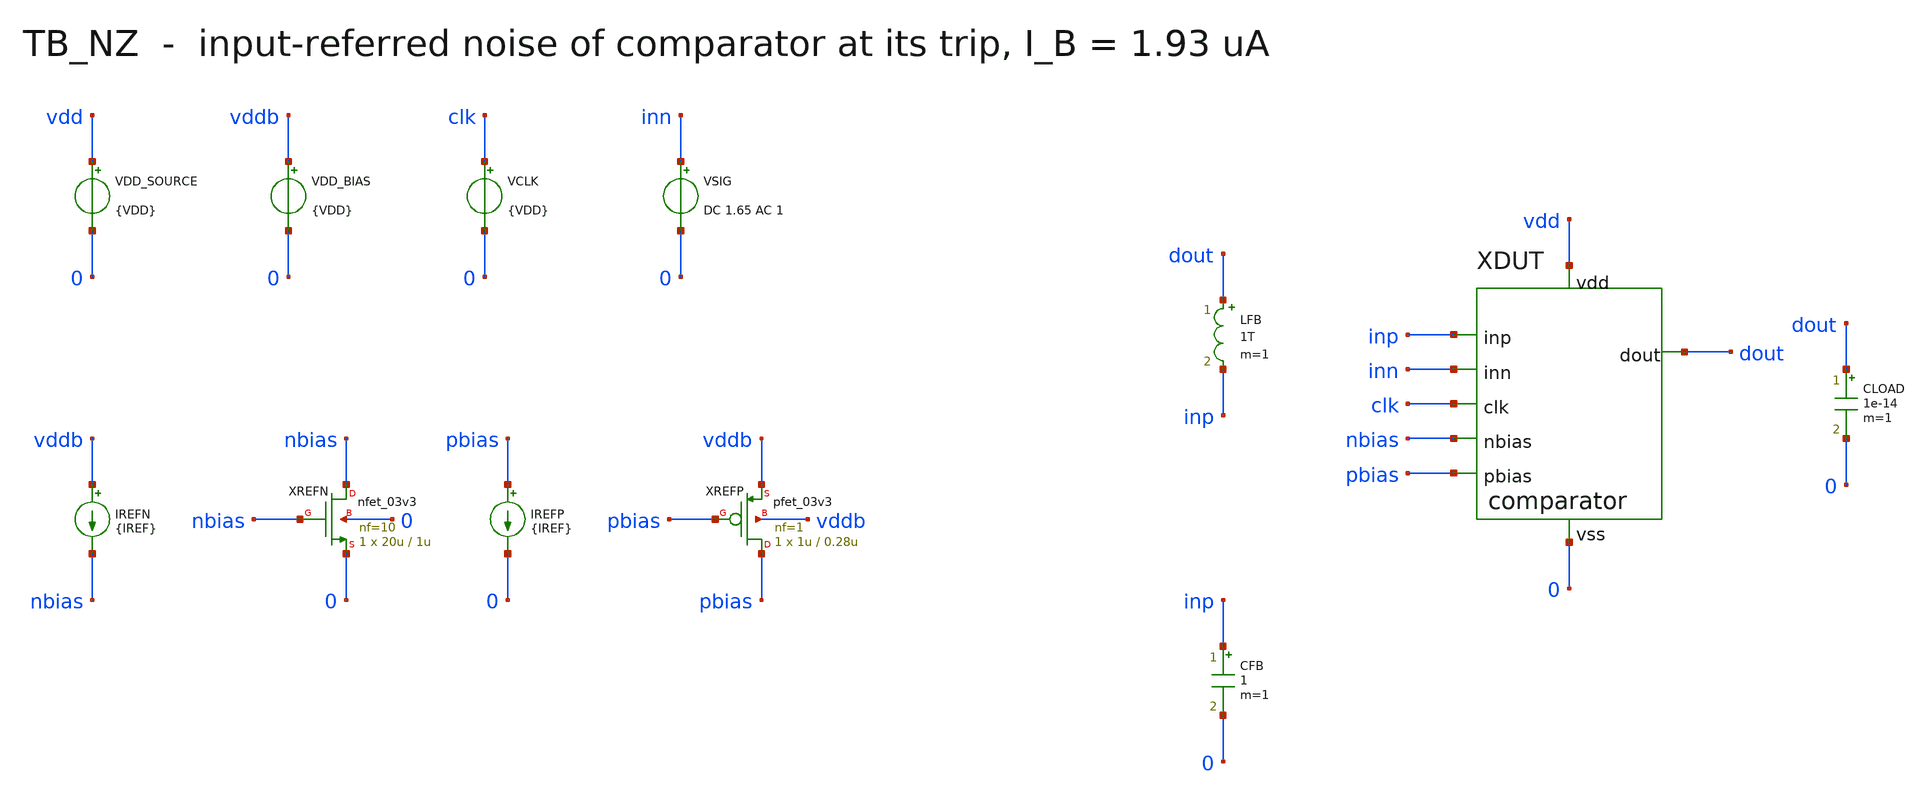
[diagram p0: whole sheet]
** sch_path: mixed_signal/comparator/tb_nz.sch
**.subckt tb_nz
VDD_SOURCE vdd 0 {VDD}
VDD_BIAS vddb 0 {VDD}
IREFN vddb nbias {IREF}
XREFN nbias nbias 0 0 nfet_03v3 L=1u W=20u nf=10 ad='int((nf+1)/2) * W/nf * 0.18u' as='int((nf+2)/2) * W/nf * 0.18u'
+ pd='2*int((nf+1)/2) * (W/nf + 0.18u)' ps='2*int((nf+2)/2) * (W/nf + 0.18u)' nrd='0.18u / W' nrs='0.18u / W'
+ sa=0 sb=0 sd=0 m=1
IREFP pbias 0 {IREF}
XREFP pbias pbias vddb vddb pfet_03v3 L=0.28u W=1u nf=1 ad='int((nf+1)/2) * W/nf * 0.18u' as='int((nf+2)/2) * W/nf * 0.18u'
+ pd='2*int((nf+1)/2) * (W/nf + 0.18u)' ps='2*int((nf+2)/2) * (W/nf + 0.18u)' nrd='0.18u / W' nrs='0.18u / W'
+ sa=0 sb=0 sd=0 m=1
VCLK clk 0 {VDD}
VSIG inn 0 DC 1.65 AC 1
CFB inp 0 1 m=1
LFB dout inp 1T m=1
XDUT inp inn dout clk vdd 0 nbias pbias comparator
CLOAD dout 0 1e-14 m=1
**** begin user architecture code

.include /foss/pdks/gf180mcuD/libs.tech/ngspice/design.ngspice
.lib /foss/pdks/gf180mcuD/libs.tech/ngspice/sm141064.ngspice typical
.param VDD=3.3
.temp 27
.param IREF=1.93077e-06
.options savecurrents
.control
op
let op_i_vdd = -i(vdd_source)
echo RESULT_BEGIN
print op_i_vdd
ac dec 20 10 100G
meas ac ota_gain_vv find vm(xdut.outa) at=10
let g3 = ota_gain_vv / sqrt(2)
meas ac ota_pole_hz when vm(xdut.outa)=$&g3 fall=1
meas ac ota_ugbw_hz when vm(xdut.outa)=1 fall=1
print ota_gain_vv
print ota_pole_hz
set g = $&ota_gain_vv
set ugb = $&ota_ugbw_hz
noise v(xdut.outa) vsig dec 20 1k 10G
let nz_own_vin = onoise_total / $g
print nz_own_vin
noise v(xdut.outa) vsig dec 20 1k 100k
let nz_lo_vin = onoise_total / $g
print nz_lo_vin
noise v(xdut.outa) vsig dec 20 1k $ugb
let nz_ugb_vin = inoise_total
print nz_ugb_vin
echo RESULT_END
quit
.endc

**** end user architecture code
**.ends

* expanding   symbol:  comparator.sym # of pins=8
** sym_path: mixed_signal/comparator/comparator.sym
** sch_path: mixed_signal/comparator/comparator.sch
.subckt comparator inp inn dout clk vdd vss nbias pbias
*.iopin vdd
*.iopin vss
*.ipin pbias
*.ipin inp
*.ipin inn
*.opin dout
*.ipin clk
*.ipin nbias
XINP left inp tail vdd pfet_03v3 L=0.32u W=12u nf=12 ad='int((nf+1)/2) * W/nf * 0.18u' as='int((nf+2)/2) * W/nf * 0.18u'
+ pd='2*int((nf+1)/2) * (W/nf + 0.18u)' ps='2*int((nf+2)/2) * (W/nf + 0.18u)' nrd='0.18u / W' nrs='0.18u / W'
+ sa=0 sb=0 sd=0 m=1
XINN outa inn tail vdd pfet_03v3 L=0.32u W=12u nf=12 ad='int((nf+1)/2) * W/nf * 0.18u' as='int((nf+2)/2) * W/nf * 0.18u'
+ pd='2*int((nf+1)/2) * (W/nf + 0.18u)' ps='2*int((nf+2)/2) * (W/nf + 0.18u)' nrd='0.18u / W' nrs='0.18u / W'
+ sa=0 sb=0 sd=0 m=1
XLOADD left left vss vss nfet_03v3 L=0.36u W=0.5u nf=1 ad='int((nf+1)/2) * W/nf * 0.18u' as='int((nf+2)/2) * W/nf * 0.18u'
+ pd='2*int((nf+1)/2) * (W/nf + 0.18u)' ps='2*int((nf+2)/2) * (W/nf + 0.18u)' nrd='0.18u / W' nrs='0.18u / W'
+ sa=0 sb=0 sd=0 m=1
XLOADM outa left vss vss nfet_03v3 L=0.36u W=0.5u nf=1 ad='int((nf+1)/2) * W/nf * 0.18u' as='int((nf+2)/2) * W/nf * 0.18u'
+ pd='2*int((nf+1)/2) * (W/nf + 0.18u)' ps='2*int((nf+2)/2) * (W/nf + 0.18u)' nrd='0.18u / W' nrs='0.18u / W'
+ sa=0 sb=0 sd=0 m=1
XTAIL tail pbias vdd vdd pfet_03v3 L=0.28u W=11u nf=11 ad='int((nf+1)/2) * W/nf * 0.18u' as='int((nf+2)/2) * W/nf * 0.18u'
+ pd='2*int((nf+1)/2) * (W/nf + 0.18u)' ps='2*int((nf+2)/2) * (W/nf + 0.18u)' nrd='0.18u / W' nrs='0.18u / W'
+ sa=0 sb=0 sd=0 m=1
XBST bst pbias vdd vdd pfet_03v3 L=0.28u W=5u nf=5 ad='int((nf+1)/2) * W/nf * 0.18u' as='int((nf+2)/2) * W/nf * 0.18u'
+ pd='2*int((nf+1)/2) * (W/nf + 0.18u)' ps='2*int((nf+2)/2) * (W/nf + 0.18u)' nrd='0.18u / W' nrs='0.18u / W'
+ sa=0 sb=0 sd=0 m=1
XBUF1 outb outa vss vss nfet_03v3 L=0.36u W=0.5u nf=1 ad='int((nf+1)/2) * W/nf * 0.18u' as='int((nf+2)/2) * W/nf * 0.18u'
+ pd='2*int((nf+1)/2) * (W/nf + 0.18u)' ps='2*int((nf+2)/2) * (W/nf + 0.18u)' nrd='0.18u / W' nrs='0.18u / W'
+ sa=0 sb=0 sd=0 m=1
XBUF2 outb outa bst vdd pfet_03v3 L=0.36u W=1u nf=1 ad='int((nf+1)/2) * W/nf * 0.18u' as='int((nf+2)/2) * W/nf * 0.18u'
+ pd='2*int((nf+1)/2) * (W/nf + 0.18u)' ps='2*int((nf+2)/2) * (W/nf + 0.18u)' nrd='0.18u / W' nrs='0.18u / W'
+ sa=0 sb=0 sd=0 m=1
XBUF3 outc outb vss vss nfet_03v3 L=0.36u W=0.5u nf=1 ad='int((nf+1)/2) * W/nf * 0.18u' as='int((nf+2)/2) * W/nf * 0.18u'
+ pd='2*int((nf+1)/2) * (W/nf + 0.18u)' ps='2*int((nf+2)/2) * (W/nf + 0.18u)' nrd='0.18u / W' nrs='0.18u / W'
+ sa=0 sb=0 sd=0 m=1
XBUF4 outc outb vdd vdd pfet_03v3 L=0.36u W=1u nf=1 ad='int((nf+1)/2) * W/nf * 0.18u' as='int((nf+2)/2) * W/nf * 0.18u'
+ pd='2*int((nf+1)/2) * (W/nf + 0.18u)' ps='2*int((nf+2)/2) * (W/nf + 0.18u)' nrd='0.18u / W' nrs='0.18u / W'
+ sa=0 sb=0 sd=0 m=1
XBUF5 dout outc vss vss nfet_03v3 L=0.36u W=0.5u nf=1 ad='int((nf+1)/2) * W/nf * 0.18u' as='int((nf+2)/2) * W/nf * 0.18u'
+ pd='2*int((nf+1)/2) * (W/nf + 0.18u)' ps='2*int((nf+2)/2) * (W/nf + 0.18u)' nrd='0.18u / W' nrs='0.18u / W'
+ sa=0 sb=0 sd=0 m=1
XBUF6 dout outc vdd vdd pfet_03v3 L=0.36u W=1u nf=1 ad='int((nf+1)/2) * W/nf * 0.18u' as='int((nf+2)/2) * W/nf * 0.18u'
+ pd='2*int((nf+1)/2) * (W/nf + 0.18u)' ps='2*int((nf+2)/2) * (W/nf + 0.18u)' nrd='0.18u / W' nrs='0.18u / W'
+ sa=0 sb=0 sd=0 m=1
.ends

.end
